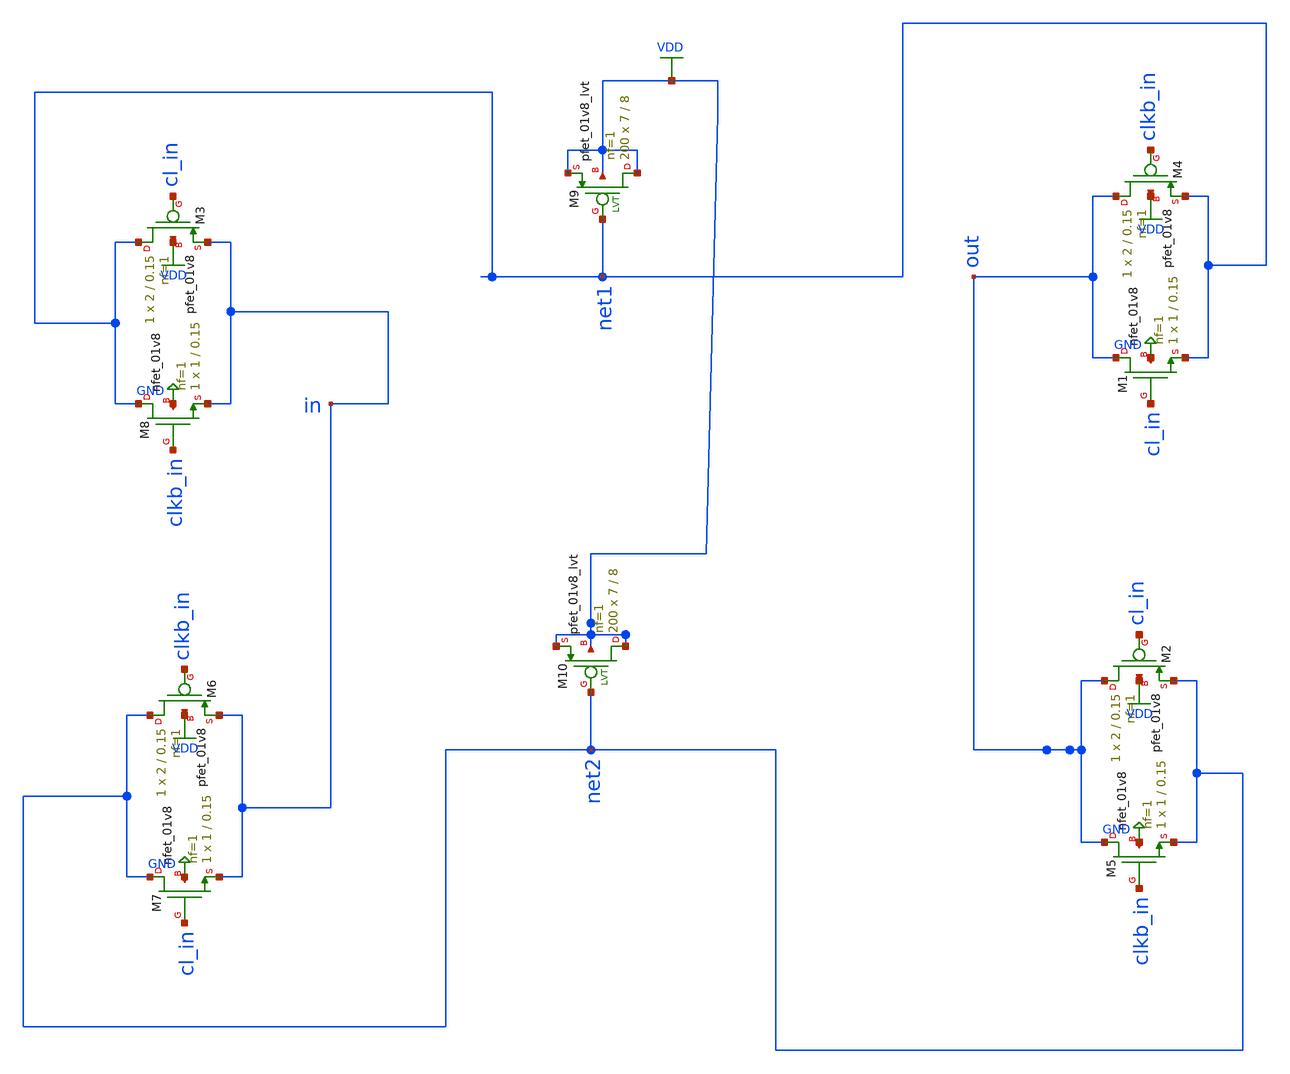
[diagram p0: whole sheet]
** sch_path: Schematics/Switched capacitor/Switchedcapacitor.sch
**.subckt Switchedcapacitor
XM9 VDD net1 VDD VDD sky130_fd_pr__pfet_01v8_lvt L=8 W=7 nf=1 ad='int((nf+1)/2) * W/nf * 0.29' as='int((nf+2)/2) * W/nf * 0.29'
+ pd='2*int((nf+1)/2) * (W/nf + 0.29)' ps='2*int((nf+2)/2) * (W/nf + 0.29)' nrd='0.29 / W' nrs='0.29 / W'
+ sa=0 sb=0 sd=0 mult=200 m=200
XM10 VDD net2 VDD VDD sky130_fd_pr__pfet_01v8_lvt L=8 W=7 nf=1 ad='int((nf+1)/2) * W/nf * 0.29' as='int((nf+2)/2) * W/nf * 0.29'
+ pd='2*int((nf+1)/2) * (W/nf + 0.29)' ps='2*int((nf+2)/2) * (W/nf + 0.29)' nrd='0.29 / W' nrs='0.29 / W'
+ sa=0 sb=0 sd=0 mult=200 m=200
XM7 net2 cl_in in GND sky130_fd_pr__nfet_01v8 L=0.15 W=1 nf=1 ad='int((nf+1)/2) * W/nf * 0.29' as='int((nf+2)/2) * W/nf * 0.29'
+ pd='2*int((nf+1)/2) * (W/nf + 0.29)' ps='2*int((nf+2)/2) * (W/nf + 0.29)' nrd='0.29 / W' nrs='0.29 / W'
+ sa=0 sb=0 sd=0 mult=1 m=1
XM5 out clkb_in net2 GND sky130_fd_pr__nfet_01v8 L=0.15 W=1 nf=1 ad='int((nf+1)/2) * W/nf * 0.29' as='int((nf+2)/2) * W/nf * 0.29'
+ pd='2*int((nf+1)/2) * (W/nf + 0.29)' ps='2*int((nf+2)/2) * (W/nf + 0.29)' nrd='0.29 / W' nrs='0.29 / W'
+ sa=0 sb=0 sd=0 mult=1 m=1
XM1 out cl_in net1 GND sky130_fd_pr__nfet_01v8 L=0.15 W=1 nf=1 ad='int((nf+1)/2) * W/nf * 0.29' as='int((nf+2)/2) * W/nf * 0.29'
+ pd='2*int((nf+1)/2) * (W/nf + 0.29)' ps='2*int((nf+2)/2) * (W/nf + 0.29)' nrd='0.29 / W' nrs='0.29 / W'
+ sa=0 sb=0 sd=0 mult=1 m=1
XM3 net1 cl_in in VDD sky130_fd_pr__pfet_01v8 L=0.15 W=2 nf=1 ad='int((nf+1)/2) * W/nf * 0.29' as='int((nf+2)/2) * W/nf * 0.29'
+ pd='2*int((nf+1)/2) * (W/nf + 0.29)' ps='2*int((nf+2)/2) * (W/nf + 0.29)' nrd='0.29 / W' nrs='0.29 / W'
+ sa=0 sb=0 sd=0 mult=1 m=1
XM4 out clkb_in net1 VDD sky130_fd_pr__pfet_01v8 L=0.15 W=2 nf=1 ad='int((nf+1)/2) * W/nf * 0.29' as='int((nf+2)/2) * W/nf * 0.29'
+ pd='2*int((nf+1)/2) * (W/nf + 0.29)' ps='2*int((nf+2)/2) * (W/nf + 0.29)' nrd='0.29 / W' nrs='0.29 / W'
+ sa=0 sb=0 sd=0 mult=1 m=1
XM6 net2 clkb_in in VDD sky130_fd_pr__pfet_01v8 L=0.15 W=2 nf=1 ad='int((nf+1)/2) * W/nf * 0.29' as='int((nf+2)/2) * W/nf * 0.29'
+ pd='2*int((nf+1)/2) * (W/nf + 0.29)' ps='2*int((nf+2)/2) * (W/nf + 0.29)' nrd='0.29 / W' nrs='0.29 / W'
+ sa=0 sb=0 sd=0 mult=1 m=1
XM2 out cl_in net2 VDD sky130_fd_pr__pfet_01v8 L=0.15 W=2 nf=1 ad='int((nf+1)/2) * W/nf * 0.29' as='int((nf+2)/2) * W/nf * 0.29'
+ pd='2*int((nf+1)/2) * (W/nf + 0.29)' ps='2*int((nf+2)/2) * (W/nf + 0.29)' nrd='0.29 / W' nrs='0.29 / W'
+ sa=0 sb=0 sd=0 mult=1 m=1
XM8 net1 clkb_in in GND sky130_fd_pr__nfet_01v8 L=0.15 W=1 nf=1 ad='int((nf+1)/2) * W/nf * 0.29' as='int((nf+2)/2) * W/nf * 0.29'
+ pd='2*int((nf+1)/2) * (W/nf + 0.29)' ps='2*int((nf+2)/2) * (W/nf + 0.29)' nrd='0.29 / W' nrs='0.29 / W'
+ sa=0 sb=0 sd=0 mult=1 m=1
**.ends
.GLOBAL GND
.GLOBAL VDD
.end
